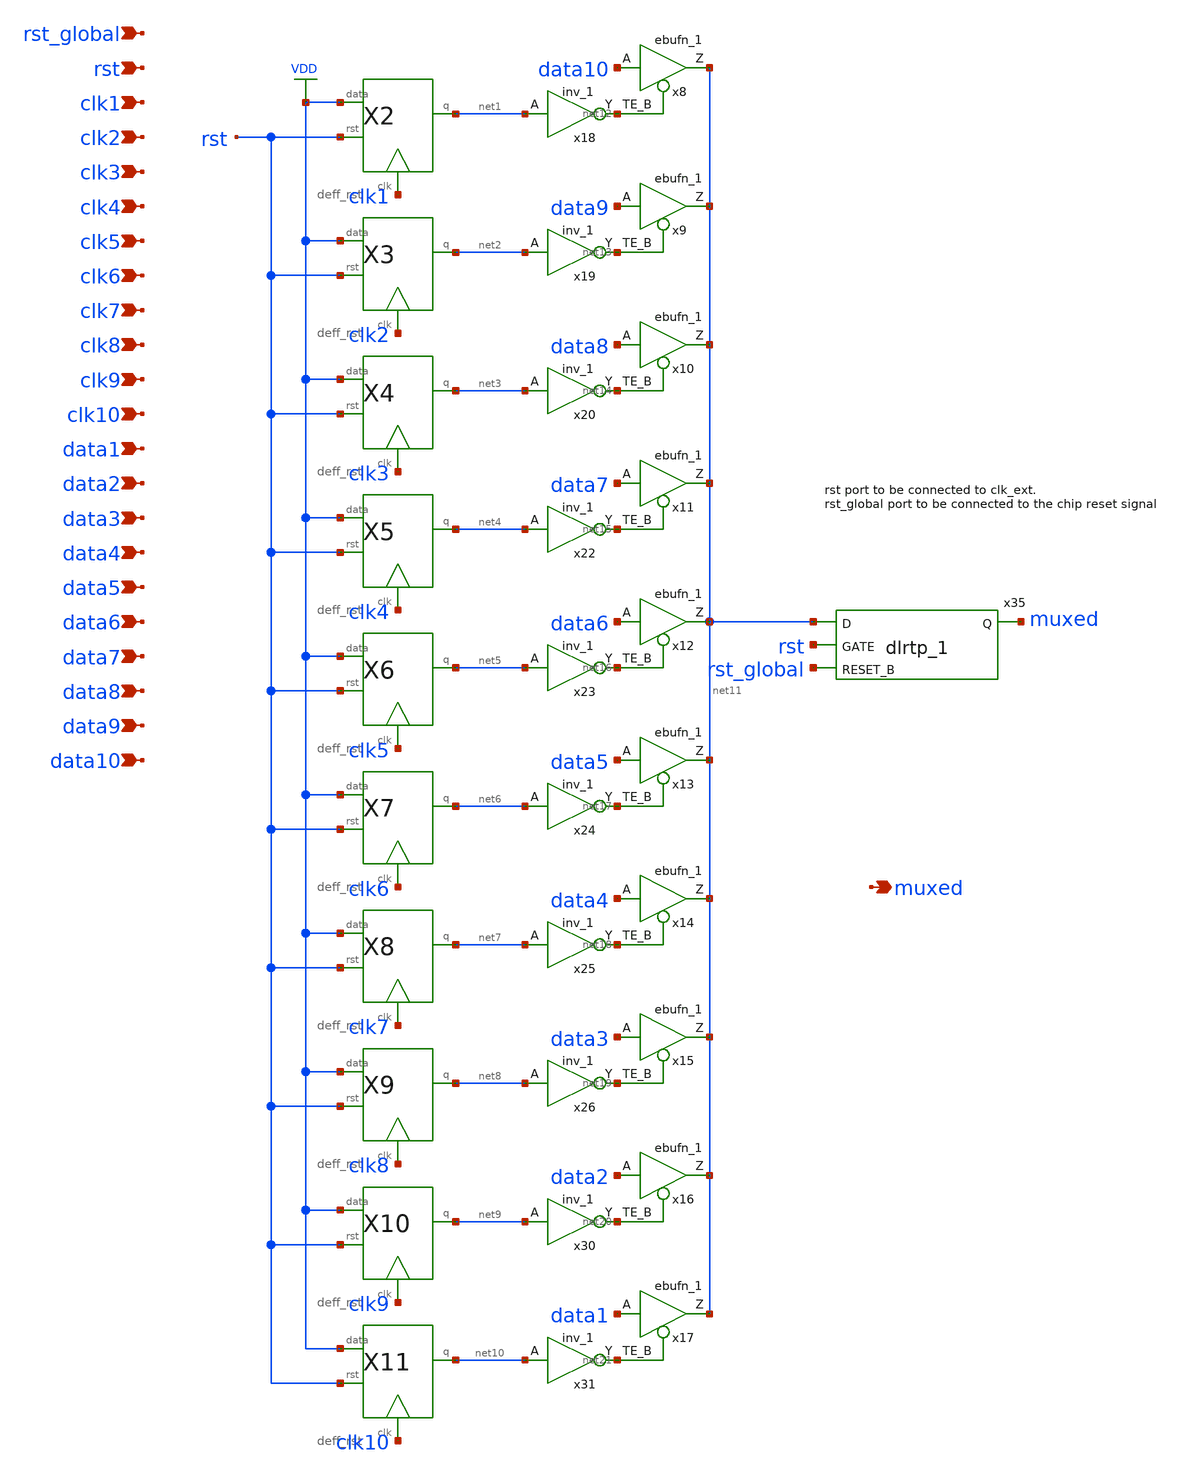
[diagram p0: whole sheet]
** sch_path: xschem/tryandtest/archive/selector_gray.sch
**.subckt selector_gray rst clk1 clk2 clk3 clk4 clk5 clk6 clk7 clk8 clk9 clk10 data1 data2 data3
*+ data4 data5 data6 data7 data8 data9 data10 muxed rst_global
*.ipin rst
*.ipin clk1
*.ipin clk2
*.ipin clk3
*.ipin clk4
*.ipin clk5
*.ipin clk6
*.ipin clk7
*.ipin clk8
*.ipin clk9
*.ipin clk10
*.ipin data1
*.ipin data2
*.ipin data3
*.ipin data4
*.ipin data5
*.ipin data6
*.ipin data7
*.ipin data8
*.ipin data9
*.ipin data10
*.opin muxed
*.ipin rst_global
X2 VDD clk1 net1 rst deff_rst
X3 VDD clk2 net2 rst deff_rst
X4 VDD clk3 net3 rst deff_rst
X5 VDD clk4 net4 rst deff_rst
X6 VDD clk5 net5 rst deff_rst
X7 VDD clk6 net6 rst deff_rst
X8 VDD clk7 net7 rst deff_rst
X9 VDD clk8 net8 rst deff_rst
X10 VDD clk9 net9 rst deff_rst
X11 VDD clk10 net10 rst deff_rst
x8 data10 net12 GND GND VDD VDD net11 sky130_fd_sc_lp__ebufn_1
x9 data9 net13 GND GND VDD VDD net11 sky130_fd_sc_lp__ebufn_1
x10 data8 net14 GND GND VDD VDD net11 sky130_fd_sc_lp__ebufn_1
x11 data7 net15 GND GND VDD VDD net11 sky130_fd_sc_lp__ebufn_1
x12 data6 net16 GND GND VDD VDD net11 sky130_fd_sc_lp__ebufn_1
x13 data5 net17 GND GND VDD VDD net11 sky130_fd_sc_lp__ebufn_1
x14 data4 net18 GND GND VDD VDD net11 sky130_fd_sc_lp__ebufn_1
x15 data3 net19 GND GND VDD VDD net11 sky130_fd_sc_lp__ebufn_1
x16 data2 net20 GND GND VDD VDD net11 sky130_fd_sc_lp__ebufn_1
x17 data1 net21 GND GND VDD VDD net11 sky130_fd_sc_lp__ebufn_1
x18 net1 GND GND VDD VDD net12 sky130_fd_sc_lp__inv_1
x19 net2 GND GND VDD VDD net13 sky130_fd_sc_lp__inv_1
x20 net3 GND GND VDD VDD net14 sky130_fd_sc_lp__inv_1
x22 net4 GND GND VDD VDD net15 sky130_fd_sc_lp__inv_1
x23 net5 GND GND VDD VDD net16 sky130_fd_sc_lp__inv_1
x24 net6 GND GND VDD VDD net17 sky130_fd_sc_lp__inv_1
x25 net7 GND GND VDD VDD net18 sky130_fd_sc_lp__inv_1
x26 net8 GND GND VDD VDD net19 sky130_fd_sc_lp__inv_1
x30 net9 GND GND VDD VDD net20 sky130_fd_sc_lp__inv_1
x31 net10 GND GND VDD VDD net21 sky130_fd_sc_lp__inv_1
x35 net11 rst rst_global GND GND VDD VDD muxed sky130_fd_sc_lp__dlrtp_1
**.ends

* expanding   symbol:  tryandtest/deff_rst.sym # of pins=4
** sym_path: xschem/tryandtest/deff_rst.sym
** sch_path: xschem/tryandtest/deff_rst.sch
.subckt deff_rst data clk q rst
*.ipin clk
*.ipin data
*.opin q
*.ipin rst
x3 net2 net3 clk GND GND VDD VDD q sky130_fd_sc_lp__mux2_1
x21 net1 data rst GND GND VDD VDD net2 sky130_fd_sc_lp__dfrtn_1
x2 net4 GND GND VDD VDD net1 sky130_fd_sc_lp__inv_1
x5 net5 GND GND VDD VDD net4 sky130_fd_sc_lp__inv_1
x1 net1 data rst GND GND VDD VDD net3 sky130_fd_sc_lp__dfrtp_1
x4 net6 GND GND VDD VDD net5 sky130_fd_sc_lp__inv_1
x6 clk GND GND VDD VDD net6 sky130_fd_sc_lp__inv_1
.ends

.GLOBAL VDD
.end
